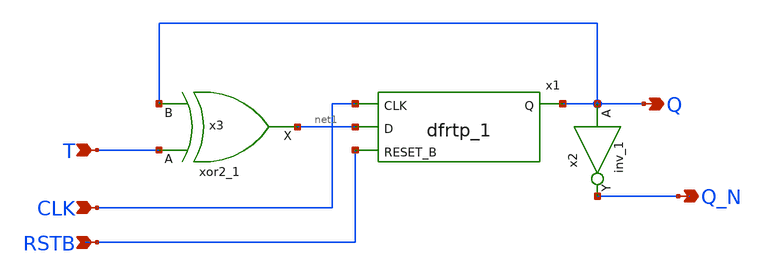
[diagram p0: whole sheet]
** sch_path: xschem/T_flip_flop/asyn_rst_t_ff.sch
**.subckt asyn_rst_t_ff T CLK Q RSTB Q_N
*.ipin T
*.ipin CLK
*.opin Q
*.ipin RSTB
*.opin Q_N
x3 T Q GND GND VDD VDD net1 sky130_fd_sc_lp__xor2_1
x2 Q GND GND VDD VDD Q_N sky130_fd_sc_lp__inv_1
x1 CLK net1 RSTB GND GND VDD VDD Q sky130_fd_sc_lp__dfrtp_1
**.ends
.end
